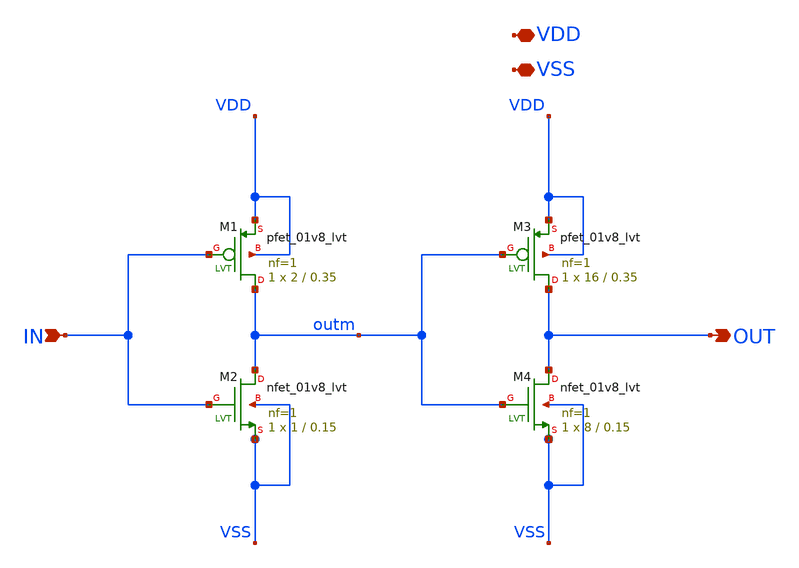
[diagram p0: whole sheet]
** sch_path: xschem/Utili/buffer_casa.sch
**.subckt buffer_casa VDD VSS IN OUT
*.iopin VDD
*.iopin VSS
*.ipin IN
*.opin OUT
XM1 outm IN VDD VDD sky130_fd_pr__pfet_01v8_lvt L=0.35 W=2 nf=1 ad='int((nf+1)/2) * W/nf * 0.29' as='int((nf+2)/2) * W/nf * 0.29'
+ pd='2*int((nf+1)/2) * (W/nf + 0.29)' ps='2*int((nf+2)/2) * (W/nf + 0.29)' nrd='0.29 / W' nrs='0.29 / W'
+ sa=0 sb=0 sd=0 mult=1 m=1
XM2 outm IN VSS VSS sky130_fd_pr__nfet_01v8_lvt L=0.15 W=1 nf=1 ad='int((nf+1)/2) * W/nf * 0.29' as='int((nf+2)/2) * W/nf * 0.29'
+ pd='2*int((nf+1)/2) * (W/nf + 0.29)' ps='2*int((nf+2)/2) * (W/nf + 0.29)' nrd='0.29 / W' nrs='0.29 / W'
+ sa=0 sb=0 sd=0 mult=1 m=1
XM3 OUT outm VDD VDD sky130_fd_pr__pfet_01v8_lvt L=0.35 W=16 nf=1 ad='int((nf+1)/2) * W/nf * 0.29' as='int((nf+2)/2) * W/nf * 0.29'
+ pd='2*int((nf+1)/2) * (W/nf + 0.29)' ps='2*int((nf+2)/2) * (W/nf + 0.29)' nrd='0.29 / W' nrs='0.29 / W'
+ sa=0 sb=0 sd=0 mult=1 m=1
XM4 OUT outm VSS VSS sky130_fd_pr__nfet_01v8_lvt L=0.15 W=8 nf=1 ad='int((nf+1)/2) * W/nf * 0.29' as='int((nf+2)/2) * W/nf * 0.29'
+ pd='2*int((nf+1)/2) * (W/nf + 0.29)' ps='2*int((nf+2)/2) * (W/nf + 0.29)' nrd='0.29 / W' nrs='0.29 / W'
+ sa=0 sb=0 sd=0 mult=1 m=1
**.ends
.end
